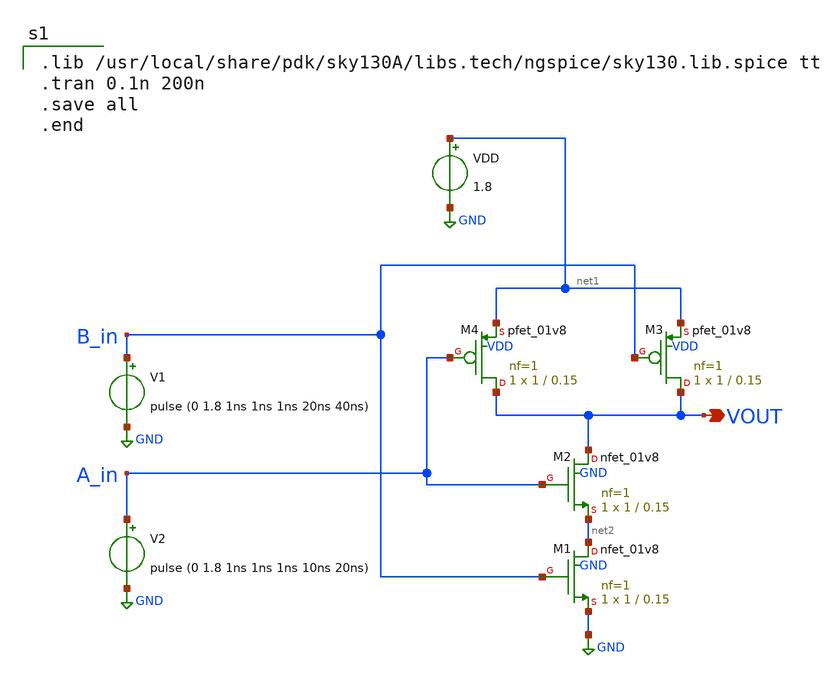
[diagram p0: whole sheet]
** sch_path: XSCHEM/nand/NAND.sch
**.subckt NAND VOUT
*.opin VOUT
XM1 net2 B_in GND GND sky130_fd_pr__nfet_01v8 L=0.15 W=1 nf=1 ad='int((nf+1)/2) * W/nf * 0.29' as='int((nf+2)/2) * W/nf * 0.29'
+ pd='2*int((nf+1)/2) * (W/nf + 0.29)' ps='2*int((nf+2)/2) * (W/nf + 0.29)' nrd='0.29 / W' nrs='0.29 / W'
+ sa=0 sb=0 sd=0 mult=1 m=1
XM2 VOUT A_in net2 GND sky130_fd_pr__nfet_01v8 L=0.15 W=1 nf=1 ad='int((nf+1)/2) * W/nf * 0.29' as='int((nf+2)/2) * W/nf * 0.29'
+ pd='2*int((nf+1)/2) * (W/nf + 0.29)' ps='2*int((nf+2)/2) * (W/nf + 0.29)' nrd='0.29 / W' nrs='0.29 / W'
+ sa=0 sb=0 sd=0 mult=1 m=1
XM3 VOUT B_in net1 VDD sky130_fd_pr__pfet_01v8 L=0.15 W=1 nf=1 ad='int((nf+1)/2) * W/nf * 0.29' as='int((nf+2)/2) * W/nf * 0.29'
+ pd='2*int((nf+1)/2) * (W/nf + 0.29)' ps='2*int((nf+2)/2) * (W/nf + 0.29)' nrd='0.29 / W' nrs='0.29 / W'
+ sa=0 sb=0 sd=0 mult=1 m=1
XM4 VOUT A_in net1 VDD sky130_fd_pr__pfet_01v8 L=0.15 W=1 nf=1 ad='int((nf+1)/2) * W/nf * 0.29' as='int((nf+2)/2) * W/nf * 0.29'
+ pd='2*int((nf+1)/2) * (W/nf + 0.29)' ps='2*int((nf+2)/2) * (W/nf + 0.29)' nrd='0.29 / W' nrs='0.29 / W'
+ sa=0 sb=0 sd=0 mult=1 m=1
VDD net1 GND 1.8
V1 B_in GND pulse (0 1.8 1ns 1ns 1ns 20ns 40ns)
V2 A_in GND pulse (0 1.8 1ns 1ns 1ns 10ns 20ns)
**** begin user architecture code

.lib /usr/local/share/pdk/sky130A/libs.tech/ngspice/sky130.lib.spice tt
.tran 0.1n 200n
.save all
.end

**** end user architecture code
**.ends
.GLOBAL GND
.end
